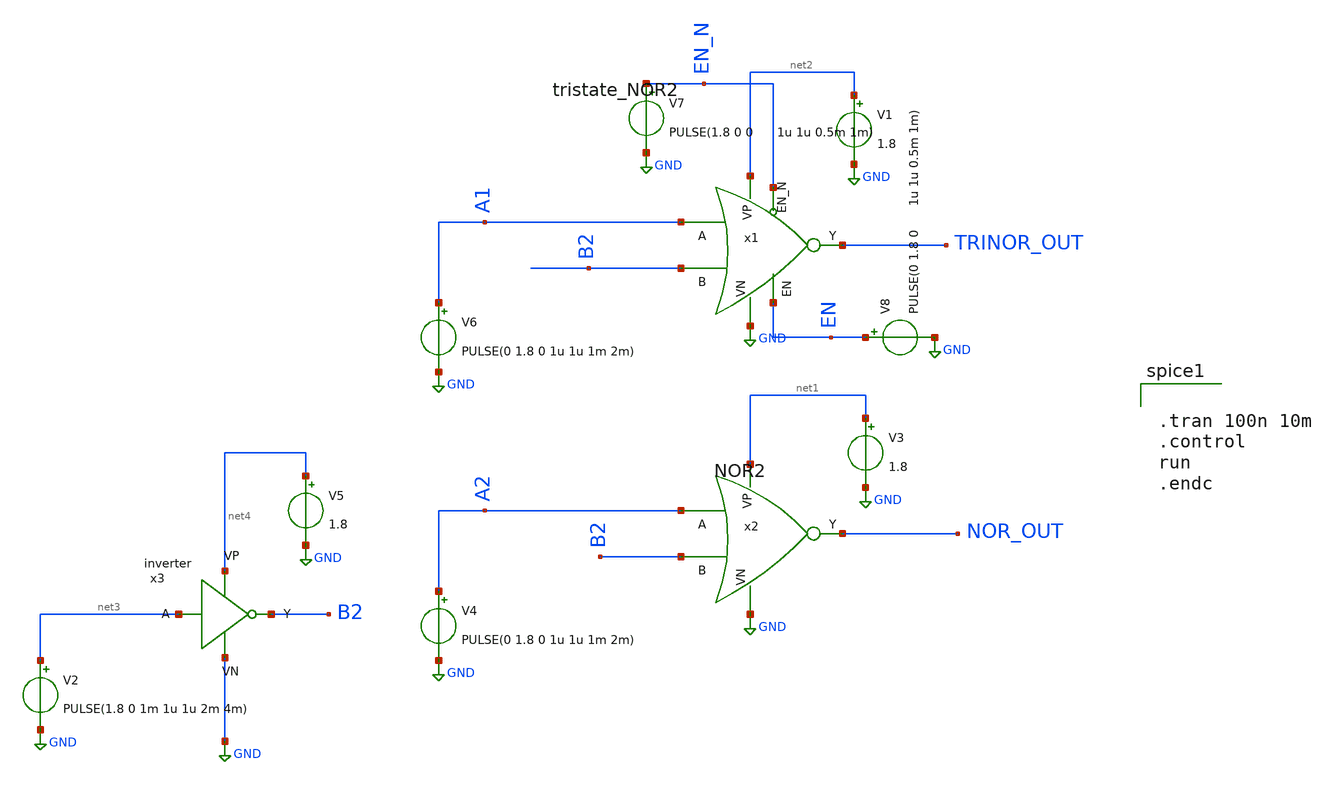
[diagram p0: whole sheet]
** sch_path: ADC/16bit_C2C/MagicAndSpice/EE431_FinalProj/nor_tb.sch
**.subckt nor_tb
x1 TRINOR_OUT net2 A1 B2 EN_N GND EN tristate_NOR2
x2 A2 B2 NOR_OUT net1 GND NOR2
V3 net1 GND 1.8
V1 net2 GND 1.8
V2 net3 GND PULSE(1.8 0 1m 1u 1u 2m 4m)
V4 A2 GND PULSE(0 1.8 0 1u 1u 1m 2m)
V6 A1 GND PULSE(0 1.8 0 1u 1u 1m 2m)
V7 EN_N GND PULSE(1.8 0 0 1u 1u 0.5m 1m)
V8 EN GND PULSE(0 1.8 0 1u 1u 0.5m 1m)
x3 net3 B2 net4 GND inverter
V5 net4 GND 1.8
**** begin user architecture code
 .lib $::SKYWATER_MODELS/sky130.lib.spice tt


.tran 100n 10m
.control
run
.endc

**** end user architecture code
**.ends
.GLOBAL GND
.end
